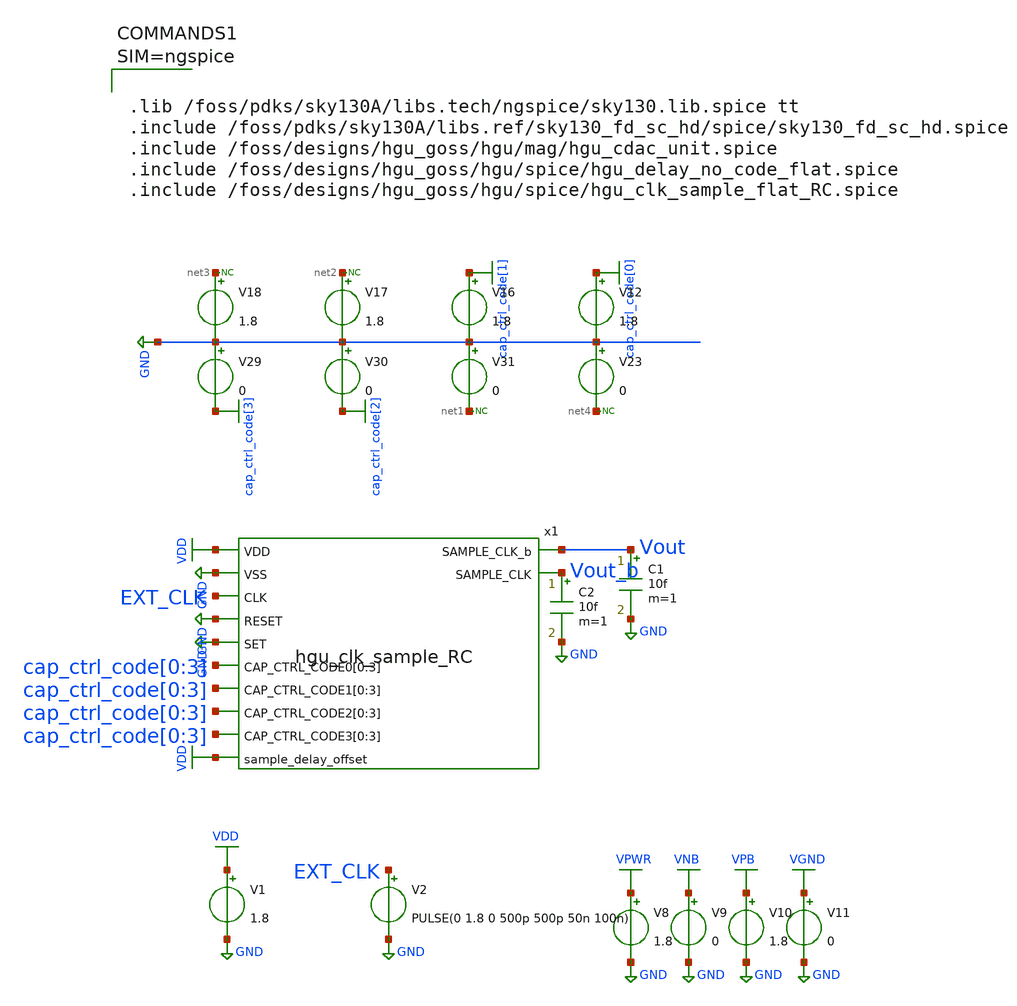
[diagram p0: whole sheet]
** sch_path: hgu/tb/tb_hgu_clk_sample.sch
**.subckt tb_hgu_clk_sample
V2 EXT_CLK GND PULSE(0 1.8 0 500p 500p 50n 100n)
V1 VDD GND 1.8
x1 Vout VDD GND EXT_CLK GND GND Vout_b cap_ctrl_code[0] cap_ctrl_code[1] cap_ctrl_code[2]
+ cap_ctrl_code[3] cap_ctrl_code[0] cap_ctrl_code[1] cap_ctrl_code[2] cap_ctrl_code[3] cap_ctrl_code[0]
+ cap_ctrl_code[1] cap_ctrl_code[2] cap_ctrl_code[3] cap_ctrl_code[0] cap_ctrl_code[1] cap_ctrl_code[2]
+ cap_ctrl_code[3] VDD hgu_clk_sample_RC
C1 Vout GND 10f m=1
V8 VPWR GND 1.8
V9 VNB GND 0
V10 VPB GND 1.8
V11 VGND GND 0
V12 cap_ctrl_code[0] GND 1.8
V29 GND cap_ctrl_code[3] 0
V30 GND cap_ctrl_code[2] 0
V31 GND net1 0
V16 cap_ctrl_code[1] GND 1.8
V17 net2 GND 1.8
V18 net3 GND 1.8
V23 GND net4 0
* noconn #net3
* noconn #net2
* noconn #net1
* noconn #net4
C2 Vout_b GND 10f m=1
**** begin user architecture code



.tran 40ps 250ns

.control
	option temp = 25
	let vdd_act = 1.8

	alter V1 vdd_act

	run
	plot V(Vout) V(Vout_b) V(EXT_CLK)+2

	let l_vdd = vdd_act * 0.2
        let h_vdd = vdd_act * 0.8
        let m_vdd = vdd_act * 0.5
        meas tran rising_s find time when V(Vout)=l_vdd RISE=1 TD=90n
        meas tran rising_e find time when V(Vout)=h_vdd RISE=1 TD=90n
        let rising_time = rising_e-rising_s
        meas tran falling_s find time when V(Vout)=h_vdd FALL=1 TD=90n
        meas tran falling_e find time when V(Vout)=l_vdd FALL=1 TD=90n
        let falling_time = falling_e-falling_s
        meas tran IN find time when V(ext_clk)=m_vdd RISE=1 TD=90n
        meas tran OUT find time when V(Vout)=m_vdd RISE=1 TD=90n
        let rising_delay = OUT-IN

	meas tran IN find time when V(Vout)=m_vdd RISE=1 TD=90n
        meas tran OUT find time when V(Vout)=m_vdd FALL=1 TD=90n
        let on_time = OUT-IN

	print rising_time falling_time rising_delay on_time
.endc
.save all






.lib /foss/pdks/sky130A/libs.tech/ngspice/sky130.lib.spice tt
.include /foss/pdks/sky130A/libs.ref/sky130_fd_sc_hd/spice/sky130_fd_sc_hd.spice
.include /foss/designs/hgu_goss/hgu/mag/hgu_cdac_unit.spice
.include /foss/designs/hgu_goss/hgu/spice/hgu_delay_no_code_flat.spice
.include /foss/designs/hgu_goss/hgu/spice/hgu_clk_sample_flat_RC.spice



**** end user architecture code
**.ends
.GLOBAL GND
.GLOBAL VDD
.GLOBAL VGND
.GLOBAL VNB
.GLOBAL VPB
.GLOBAL VPWR
.GLOBAL cap_ctrl_code[3]
.GLOBAL cap_ctrl_code[2]
.GLOBAL cap_ctrl_code[1]
.GLOBAL cap_ctrl_code[0]
.end
